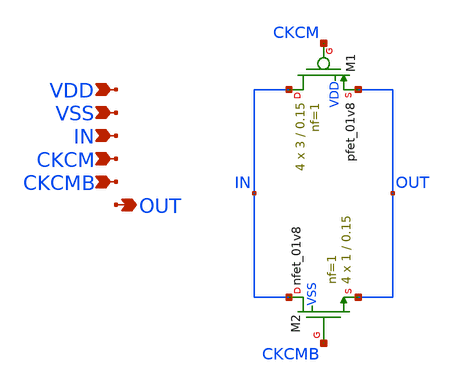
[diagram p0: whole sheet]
** sch_path: xschem/tg_sw.sch
**.subckt tg_sw VDD VSS IN CKCM CKCMB OUT
*.ipin VDD
*.ipin VSS
*.ipin IN
*.ipin CKCM
*.ipin CKCMB
*.opin OUT
XM1 IN CKCM OUT VDD sky130_fd_pr__pfet_01v8 L=0.15 W=3 nf=1 ad='int((nf+1)/2) * W/nf * 0.29' as='int((nf+2)/2) * W/nf * 0.29'
+ pd='2*int((nf+1)/2) * (W/nf + 0.29)' ps='2*int((nf+2)/2) * (W/nf + 0.29)' nrd='0.29 / W' nrs='0.29 / W'
+ sa=0 sb=0 sd=0 mult=4 m=4
XM2 IN CKCMB OUT VSS sky130_fd_pr__nfet_01v8 L=0.15 W=1 nf=1 ad='int((nf+1)/2) * W/nf *z 0.29' as='int((nf+2)/2) * W/nf * 0.29'
+ pd='2*int((nf+1)/2) * (W/nf + 0.29)' ps='2*int((nf+2)/2) * (W/nf + 0.29)' nrd='0.29 / W' nrs='0.29 / W'
+ sa=0 sb=0 sd=0 mult=4 m=4
**.ends
.end
